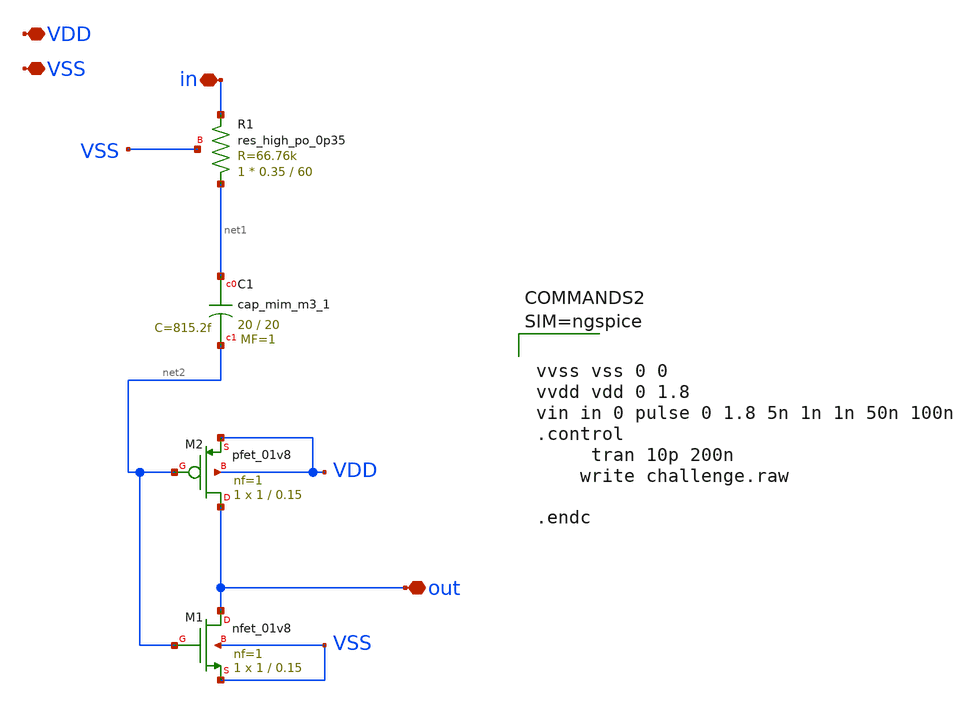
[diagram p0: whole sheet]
** sch_path: xschem/challenge.sch
**.subckt challenge out VDD VSS in
*.iopin out
*.iopin VDD
*.iopin VSS
*.iopin in
XR1 net1 in VSS sky130_fd_pr__res_high_po_0p35 L=60 mult=1 m=1
XC1 net1 net2 sky130_fd_pr__cap_mim_m3_1 W=20 L=20 MF=1 m=1
XM1 out net2 VSS VSS sky130_fd_pr__nfet_01v8 L=0.15 W=1 nf=1 ad='int((nf+1)/2) * W/nf * 0.29' as='int((nf+2)/2) * W/nf * 0.29'
+ pd='2*int((nf+1)/2) * (W/nf + 0.29)' ps='2*int((nf+2)/2) * (W/nf + 0.29)' nrd='0.29 / W' nrs='0.29 / W'
+ sa=0 sb=0 sd=0 mult=1 m=1
XM2 out net2 VDD VDD sky130_fd_pr__pfet_01v8 L=0.15 W=1 nf=1 ad='int((nf+1)/2) * W/nf * 0.29' as='int((nf+2)/2) * W/nf * 0.29'
+ pd='2*int((nf+1)/2) * (W/nf + 0.29)' ps='2*int((nf+2)/2) * (W/nf + 0.29)' nrd='0.29 / W' nrs='0.29 / W'
+ sa=0 sb=0 sd=0 mult=1 m=1
**** begin user architecture code

** opencircuitdesign pdks install
.lib $::SKYWATER_MODELS/sky130.lib.spice tt





vvss vss 0 0
vvdd vdd 0 1.8
vin in 0 pulse 0 1.8 5n 1n 1n 50n 100n
.control
     tran 10p 200n
    write challenge.raw

.endc



**** end user architecture code
**.ends
.end
